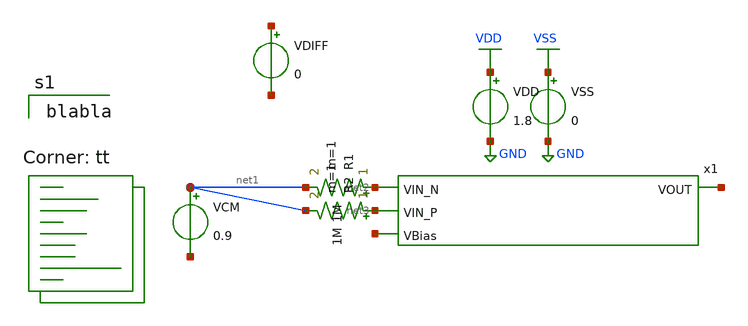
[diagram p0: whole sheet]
** sch_path: analog/schematics/tb_dc_analysis.sch
**.subckt tb_dc_analysis
x1 net2 net3 net4 net5 bootcamp_opamp
VDD net6 GND 1.8
VSS net7 GND 0
VCM net1 net8 0.9
R1 net2 net1 1M m=1
R2 net3 net1 1M m=1
VDIFF net9 net10 0
**** begin user architecture code

blabla

.lib $::SKYWATER_MODELS/sky130.lib.spice tt
**** end user architecture code
**.ends

* expanding   symbol:  bootcamp_opamp.sym # of pins=4
** sym_path: analog/schematics/bootcamp_opamp.sym
** sch_path: analog/schematics/bootcamp_opamp.sch
.subckt bootcamp_opamp VIN_N VIN_P VOUT VBias
*.ipin VIN_P
*.ipin VIN_N
*.opin VOUT
*.ipin VBias
XM1 net1 VBias VSS GND sky130_fd_pr__nfet_01v8 L=0.15 W=1 nf=1 ad='int((nf+1)/2) * W/nf * 0.29' as='int((nf+2)/2) * W/nf * 0.29'
+ pd='2*int((nf+1)/2) * (W/nf + 0.29)' ps='2*int((nf+2)/2) * (W/nf + 0.29)' nrd='0.29 / W' nrs='0.29 / W'
+ sa=0 sb=0 sd=0 mult=1 m=1
XM2 VOUT VBias VSS GND sky130_fd_pr__nfet_01v8 L=0.15 W=1 nf=1 ad='int((nf+1)/2) * W/nf * 0.29' as='int((nf+2)/2) * W/nf * 0.29'
+ pd='2*int((nf+1)/2) * (W/nf + 0.29)' ps='2*int((nf+2)/2) * (W/nf + 0.29)' nrd='0.29 / W' nrs='0.29 / W'
+ sa=0 sb=0 sd=0 mult=1 m=1
XM3 net2 VIN_N net1 GND sky130_fd_pr__nfet_01v8 L=0.15 W=1 nf=1 ad='int((nf+1)/2) * W/nf * 0.29' as='int((nf+2)/2) * W/nf * 0.29'
+ pd='2*int((nf+1)/2) * (W/nf + 0.29)' ps='2*int((nf+2)/2) * (W/nf + 0.29)' nrd='0.29 / W' nrs='0.29 / W'
+ sa=0 sb=0 sd=0 mult=1 m=1
XM4 net2 net2 VDD net5 sky130_fd_pr__pfet_01v8 L=0.15 W=1 nf=1 ad='int((nf+1)/2) * W/nf * 0.29' as='int((nf+2)/2) * W/nf * 0.29'
+ pd='2*int((nf+1)/2) * (W/nf + 0.29)' ps='2*int((nf+2)/2) * (W/nf + 0.29)' nrd='0.29 / W' nrs='0.29 / W'
+ sa=0 sb=0 sd=0 mult=1 m=1
XM5 net3 VIN_P net1 GND sky130_fd_pr__nfet_01v8 L=0.15 W=1 nf=1 ad='int((nf+1)/2) * W/nf * 0.29' as='int((nf+2)/2) * W/nf * 0.29'
+ pd='2*int((nf+1)/2) * (W/nf + 0.29)' ps='2*int((nf+2)/2) * (W/nf + 0.29)' nrd='0.29 / W' nrs='0.29 / W'
+ sa=0 sb=0 sd=0 mult=1 m=1
XM6 net3 net2 VDD net6 sky130_fd_pr__pfet_01v8 L=0.15 W=1 nf=1 ad='int((nf+1)/2) * W/nf * 0.29' as='int((nf+2)/2) * W/nf * 0.29'
+ pd='2*int((nf+1)/2) * (W/nf + 0.29)' ps='2*int((nf+2)/2) * (W/nf + 0.29)' nrd='0.29 / W' nrs='0.29 / W'
+ sa=0 sb=0 sd=0 mult=1 m=1
XM7 VOUT net3 VDD net7 sky130_fd_pr__pfet_01v8 L=0.15 W=1 nf=1 ad='int((nf+1)/2) * W/nf * 0.29' as='int((nf+2)/2) * W/nf * 0.29'
+ pd='2*int((nf+1)/2) * (W/nf + 0.29)' ps='2*int((nf+2)/2) * (W/nf + 0.29)' nrd='0.29 / W' nrs='0.29 / W'
+ sa=0 sb=0 sd=0 mult=1 m=1
R1 net3 net4 sky130_fd_pr__res_generic_li W=1 L=1 m=1
XC1 net4 VOUT sky130_fd_pr__cap_mim_m3_1 W=1 L=1 MF=1 m=1
.ends

.GLOBAL GND
.GLOBAL VDD
.GLOBAL VSS
.end
